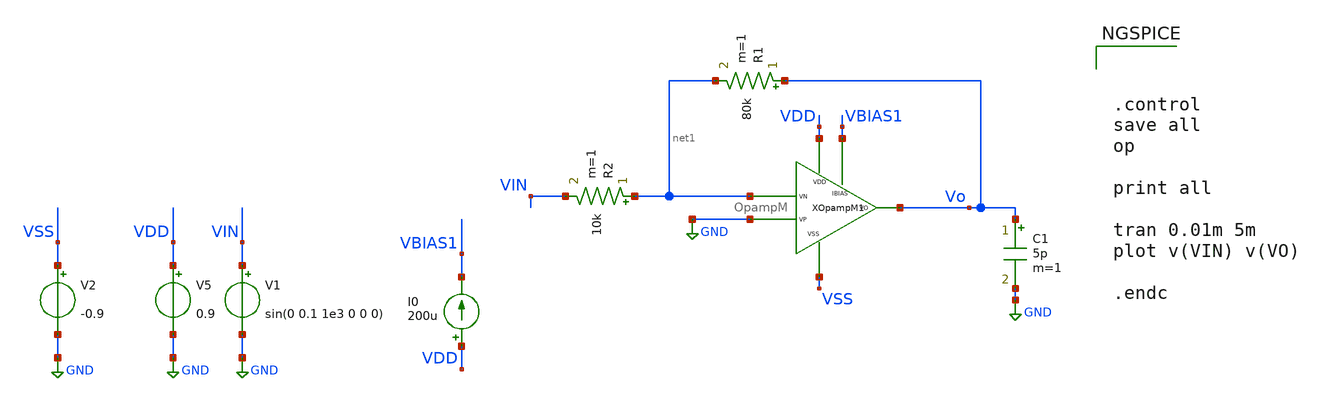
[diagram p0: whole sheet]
** sch_path: xschem/xschem_BGR_Top/Op_Amp/OpampM_tb_Tran.sch
**.subckt OpampM_tb_Tran
V1 VIN GND sin(0 0.1 1e3 0 0 0)
V5 VDD GND 0.9
I0 VDD VBIAS1 200u
R1 Vo net1 80k m=1
R2 net1 VIN 10k m=1
V2 VSS GND -0.9
C1 Vo GND 5p m=1
XOpampM1 VBIAS1 VDD net1 GND VSS Vo OpampM
**** begin user architecture code



.control
save all
op

print all

tran 0.01m 5m
plot v(VIN) v(VO)

.endc


** manual skywater pdks install (with patches applied)
* .lib $::SKYWATER_MODELS/models/sky130.lib.spice tt

** opencircuitdesign pdks install
.lib $::SKYWATER_MODELS/sky130.lib.spice tt


**** end user architecture code
**.ends

* expanding   symbol:  Sigma_Delta/Op_Amp/OpampM.sym # of pins=6
** sym_path: xschem/xschem_BGR_Top/Op_Amp/OpampM.sym
** sch_path: xschem/xschem_BGR_Top/Op_Amp/OpampM.sch
.subckt OpampM IBIAS VDD VN VP VSS VO
*.iopin VDD
*.iopin VSS
*.iopin VP
*.iopin VN
*.iopin VO
*.iopin IBIAS
XM1 net1 VN net3 VSS sky130_fd_pr__nfet_01v8 L=0.5 W=50 nf=10 ad='int((nf+1)/2) * W/nf * 0.29' as='int((nf+2)/2) * W/nf * 0.29'
+ pd='2*int((nf+1)/2) * (W/nf + 0.29)' ps='2*int((nf+2)/2) * (W/nf + 0.29)' nrd='0.29 / W' nrs='0.29 / W'
+ sa=0 sb=0 sd=0 mult=1 m=1
XM3 net1 net1 VDD VDD sky130_fd_pr__pfet_01v8_lvt L=0.5 W=60 nf=10 ad='int((nf+1)/2) * W/nf * 0.29' as='int((nf+2)/2) * W/nf * 0.29'
+ pd='2*int((nf+1)/2) * (W/nf + 0.29)' ps='2*int((nf+2)/2) * (W/nf + 0.29)' nrd='0.29 / W' nrs='0.29 / W'
+ sa=0 sb=0 sd=0 mult=1 m=1
XM2 net2 VP net3 VSS sky130_fd_pr__nfet_01v8 L=0.5 W=50 nf=10 ad='int((nf+1)/2) * W/nf * 0.29' as='int((nf+2)/2) * W/nf * 0.29'
+ pd='2*int((nf+1)/2) * (W/nf + 0.29)' ps='2*int((nf+2)/2) * (W/nf + 0.29)' nrd='0.29 / W' nrs='0.29 / W'
+ sa=0 sb=0 sd=0 mult=1 m=1
XM4 net2 net1 VDD VDD sky130_fd_pr__pfet_01v8_lvt L=0.5 W=60 nf=10 ad='int((nf+1)/2) * W/nf * 0.29' as='int((nf+2)/2) * W/nf * 0.29'
+ pd='2*int((nf+1)/2) * (W/nf + 0.29)' ps='2*int((nf+2)/2) * (W/nf + 0.29)' nrd='0.29 / W' nrs='0.29 / W'
+ sa=0 sb=0 sd=0 mult=1 m=1
XM5 net3 IBIAS VSS VSS sky130_fd_pr__nfet_01v8 L=0.5 W=21 nf=10 ad='int((nf+1)/2) * W/nf * 0.29' as='int((nf+2)/2) * W/nf * 0.29'
+ pd='2*int((nf+1)/2) * (W/nf + 0.29)' ps='2*int((nf+2)/2) * (W/nf + 0.29)' nrd='0.29 / W' nrs='0.29 / W'
+ sa=0 sb=0 sd=0 mult=1 m=1
XM7 VO IBIAS VSS VSS sky130_fd_pr__nfet_01v8 L=0.5 W=63 nf=10 ad='int((nf+1)/2) * W/nf * 0.29' as='int((nf+2)/2) * W/nf * 0.29'
+ pd='2*int((nf+1)/2) * (W/nf + 0.29)' ps='2*int((nf+2)/2) * (W/nf + 0.29)' nrd='0.29 / W' nrs='0.29 / W'
+ sa=0 sb=0 sd=0 mult=1 m=1
XM8 IBIAS IBIAS VSS VSS sky130_fd_pr__nfet_01v8 L=0.5 W=21 nf=10 ad='int((nf+1)/2) * W/nf * 0.29' as='int((nf+2)/2) * W/nf * 0.29'
+ pd='2*int((nf+1)/2) * (W/nf + 0.29)' ps='2*int((nf+2)/2) * (W/nf + 0.29)' nrd='0.29 / W' nrs='0.29 / W'
+ sa=0 sb=0 sd=0 mult=1 m=1
XC1 net2 VO sky130_fd_pr__cap_mim_m3_1 W=24 L=24 MF=1 m=1
XC2 VDD VSS sky130_fd_pr__cap_mim_m3_1 W=30 L=10 MF=1 m=1
XC3 VDD VSS sky130_fd_pr__cap_mim_m3_1 W=30 L=10 MF=1 m=1
XM6 VO net2 VDD VDD sky130_fd_pr__pfet_01v8_lvt L=0.50 W=355 nf=20 ad='int((nf+1)/2) * W/nf * 0.29' as='int((nf+2)/2) * W/nf * 0.29'
+ pd='2*int((nf+1)/2) * (W/nf + 0.29)' ps='2*int((nf+2)/2) * (W/nf + 0.29)' nrd='0.29 / W' nrs='0.29 / W'
+ sa=0 sb=0 sd=0 mult=1 m=1
.ends

.GLOBAL GND
.end
